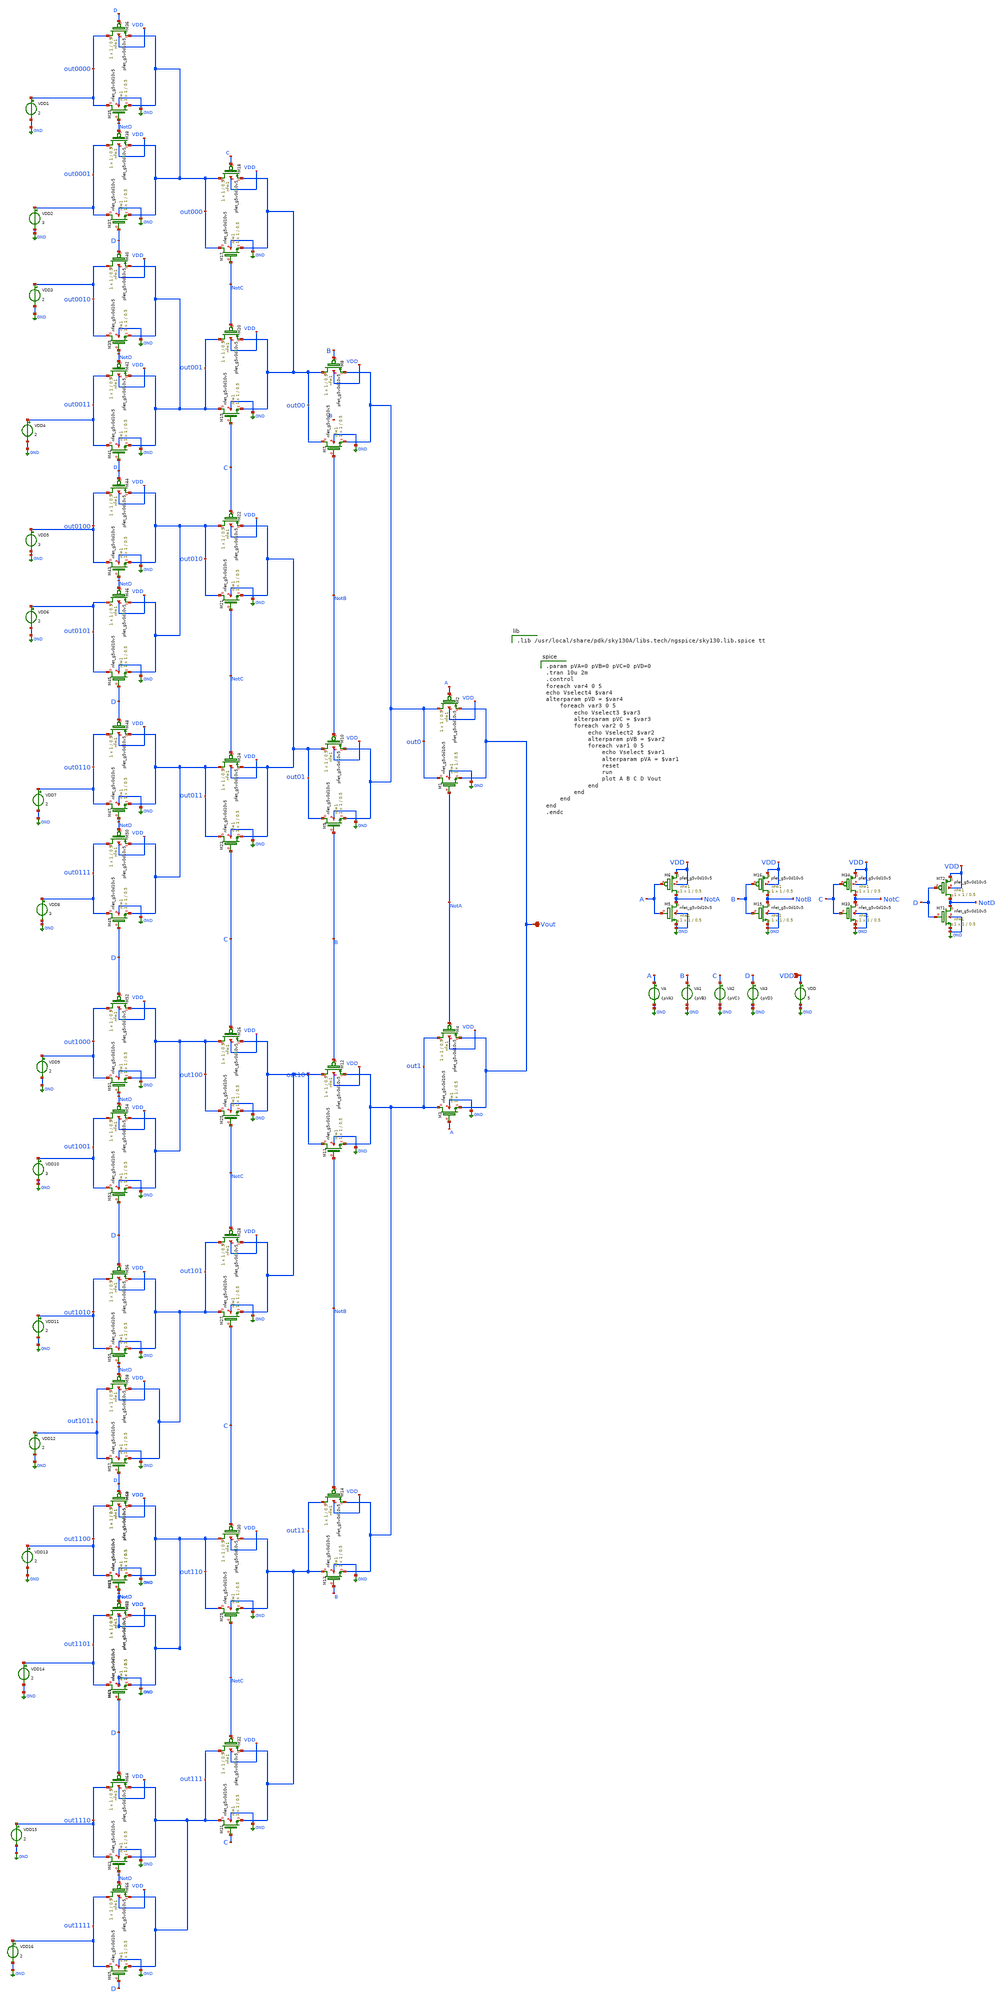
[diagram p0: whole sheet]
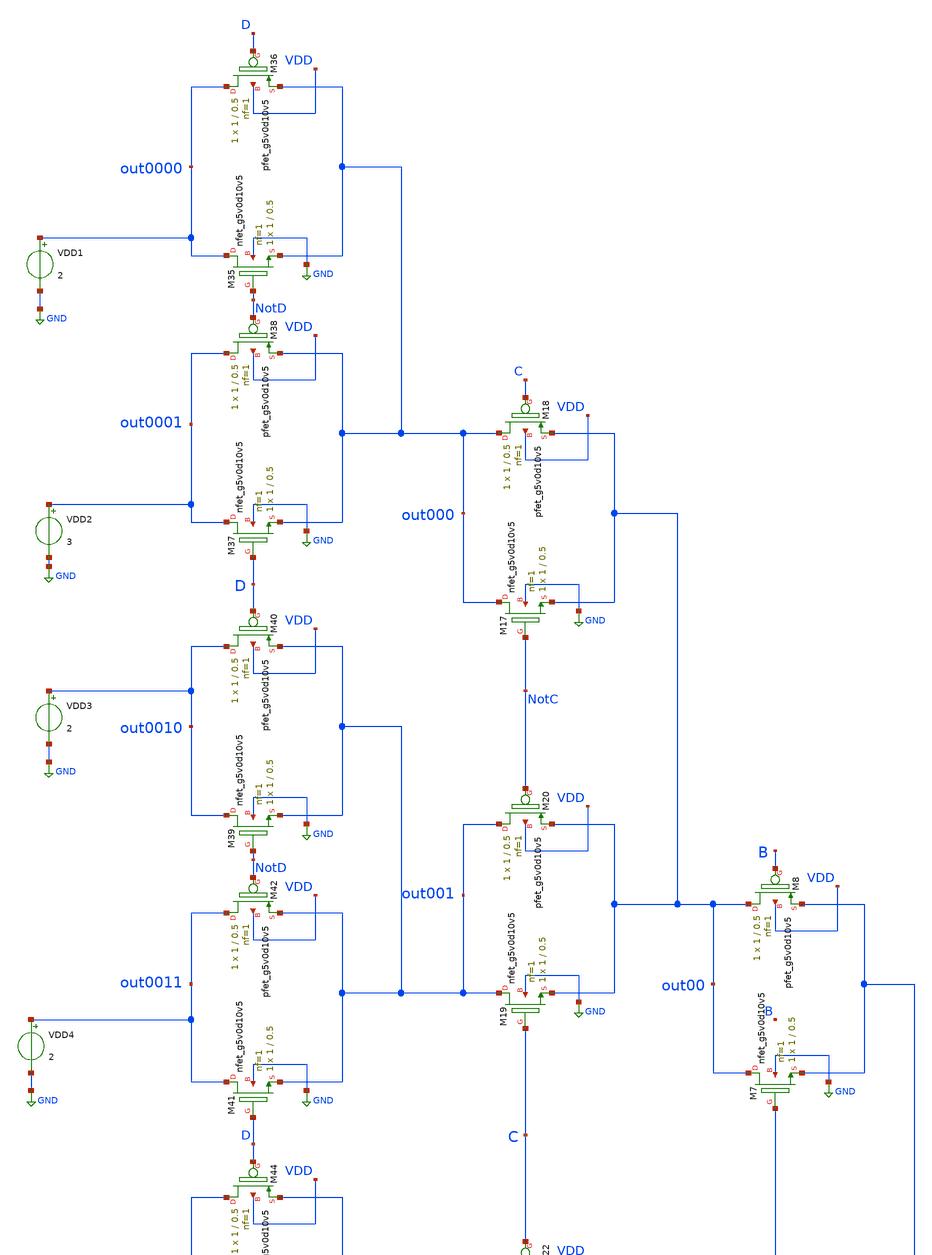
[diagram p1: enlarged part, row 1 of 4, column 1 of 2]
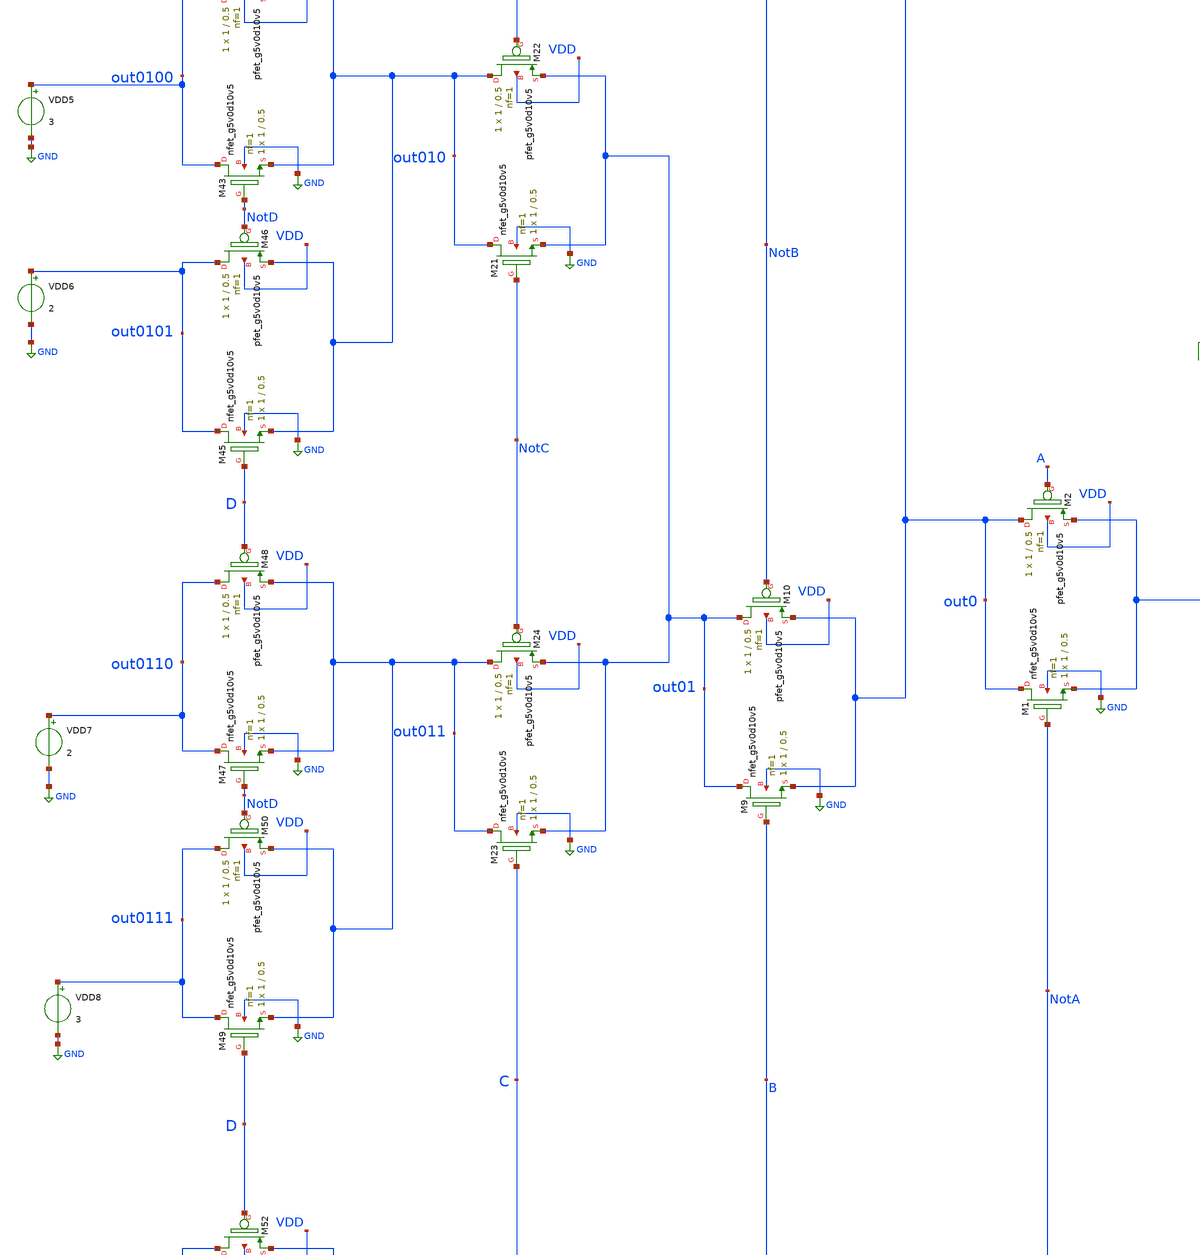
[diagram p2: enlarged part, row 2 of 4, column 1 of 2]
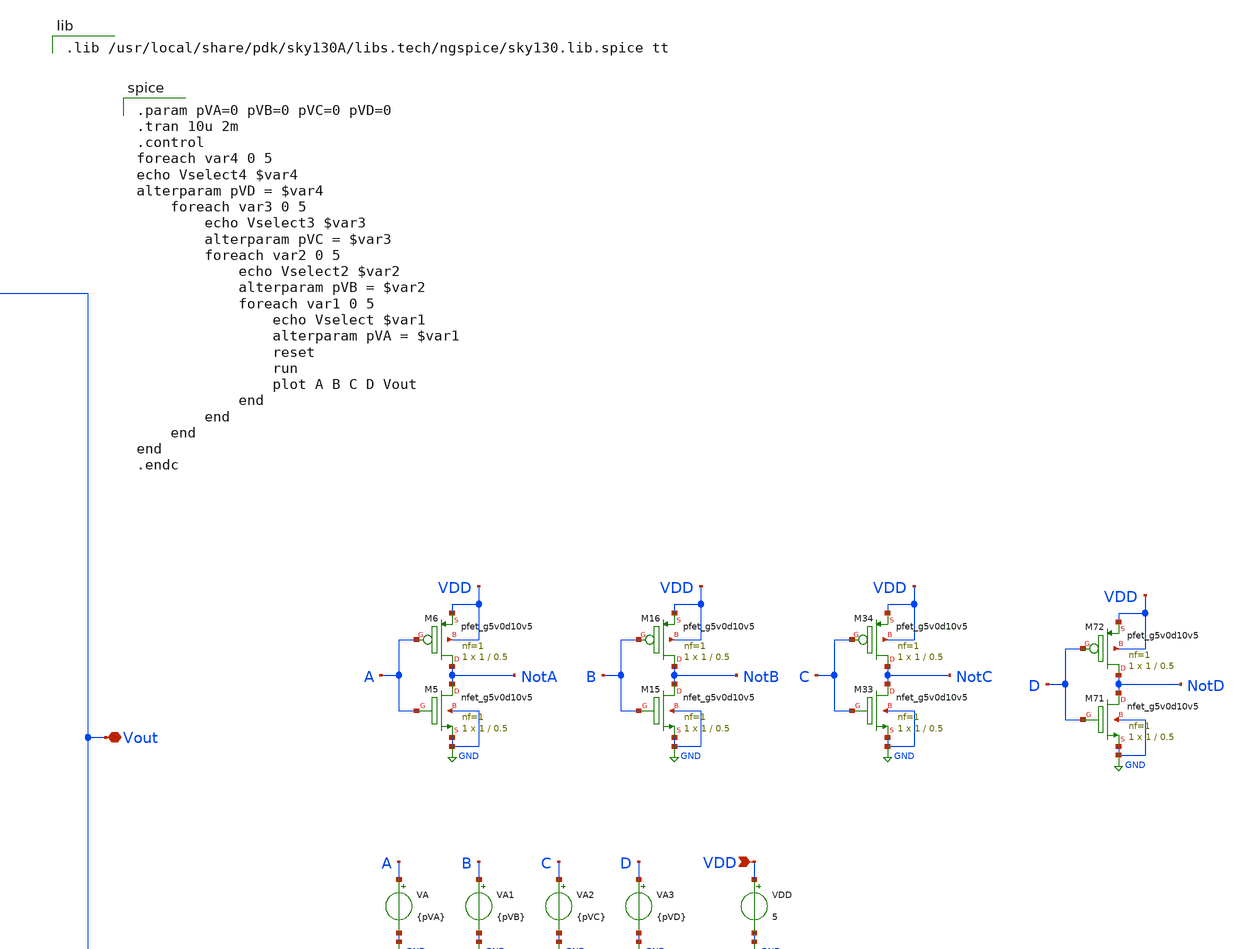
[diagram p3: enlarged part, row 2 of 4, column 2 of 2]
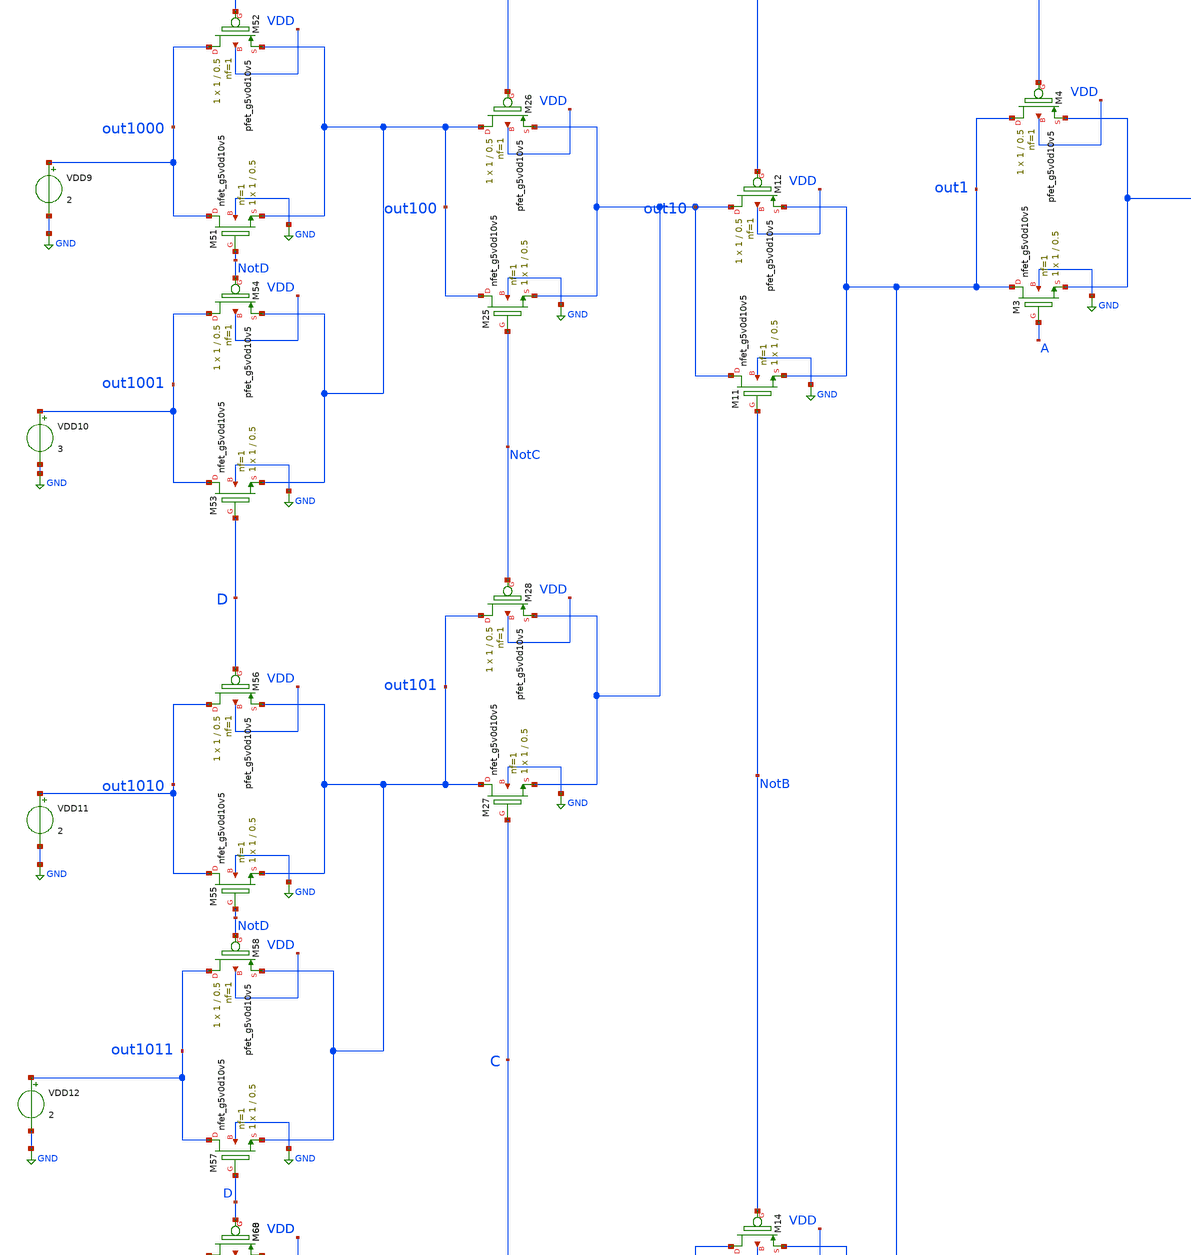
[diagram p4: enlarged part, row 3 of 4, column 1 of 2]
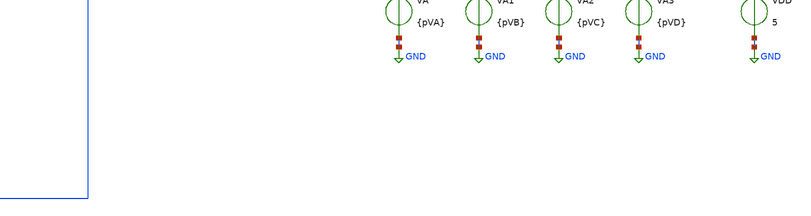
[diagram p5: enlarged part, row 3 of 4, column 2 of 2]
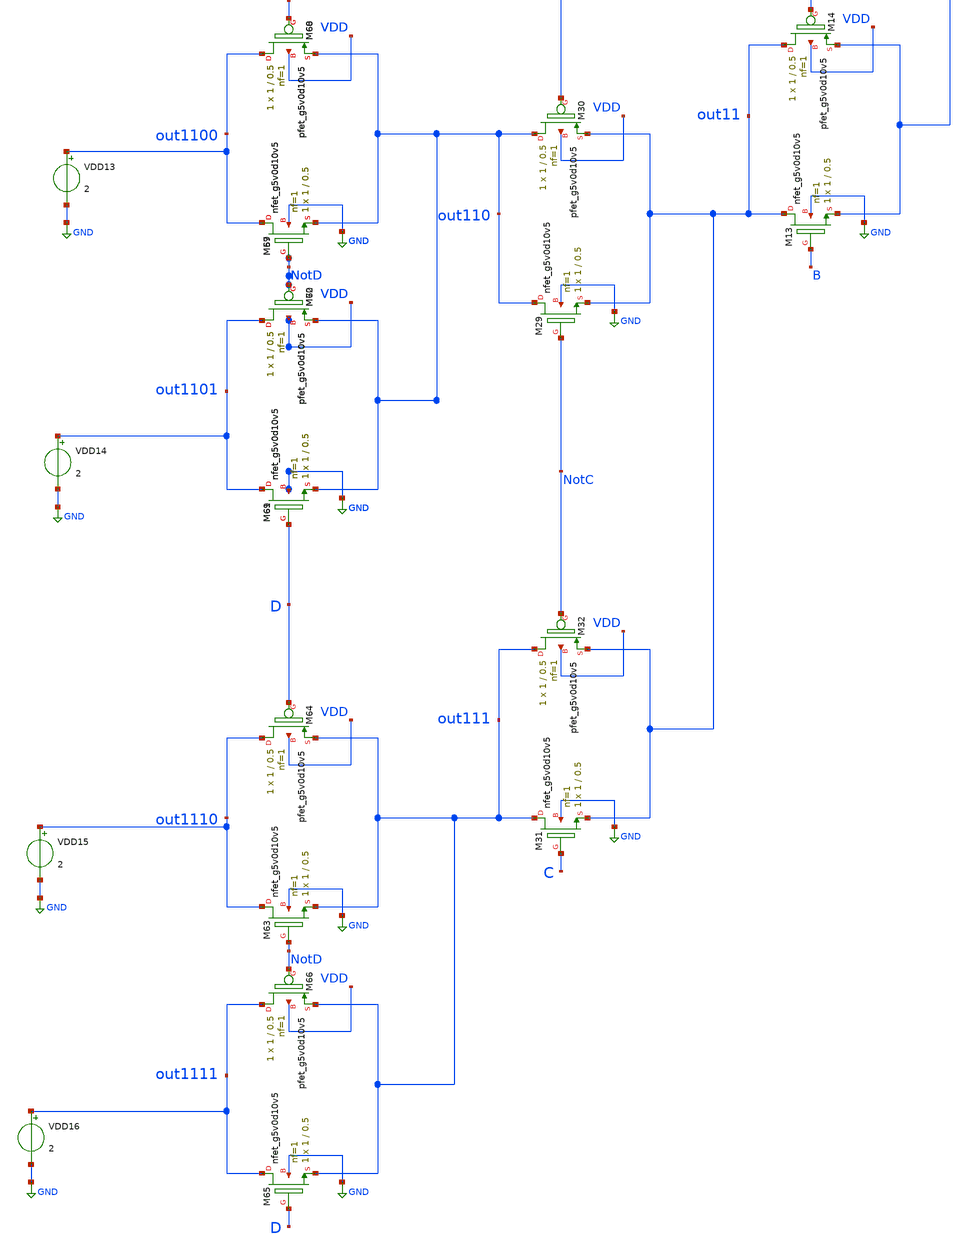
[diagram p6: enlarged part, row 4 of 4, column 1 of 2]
** sch_path: xschem/DemuxCompleto.sch
**.subckt DemuxCompleto Vout VDD
*.iopin Vout
*.ipin VDD
XM1 out0 NotA Vout GND sky130_fd_pr__nfet_g5v0d10v5 L=0.5 W=1 nf=1 ad='int((nf+1)/2) * W/nf * 0.29' as='int((nf+2)/2) * W/nf * 0.29'
+ pd='2*int((nf+1)/2) * (W/nf + 0.29)' ps='2*int((nf+2)/2) * (W/nf + 0.29)' nrd='0.29 / W' nrs='0.29 / W'
+ sa=0 sb=0 sd=0 mult=1 m=1
XM2 out0 A Vout VDD sky130_fd_pr__pfet_g5v0d10v5 L=0.5 W=1 nf=1 ad='int((nf+1)/2) * W/nf * 0.29' as='int((nf+2)/2) * W/nf * 0.29'
+ pd='2*int((nf+1)/2) * (W/nf + 0.29)' ps='2*int((nf+2)/2) * (W/nf + 0.29)' nrd='0.29 / W' nrs='0.29 / W'
+ sa=0 sb=0 sd=0 mult=1 m=1
XM3 out1 A Vout GND sky130_fd_pr__nfet_g5v0d10v5 L=0.5 W=1 nf=1 ad='int((nf+1)/2) * W/nf * 0.29' as='int((nf+2)/2) * W/nf * 0.29'
+ pd='2*int((nf+1)/2) * (W/nf + 0.29)' ps='2*int((nf+2)/2) * (W/nf + 0.29)' nrd='0.29 / W' nrs='0.29 / W'
+ sa=0 sb=0 sd=0 mult=1 m=1
XM4 out1 NotA Vout VDD sky130_fd_pr__pfet_g5v0d10v5 L=0.5 W=1 nf=1 ad='int((nf+1)/2) * W/nf * 0.29' as='int((nf+2)/2) * W/nf * 0.29'
+ pd='2*int((nf+1)/2) * (W/nf + 0.29)' ps='2*int((nf+2)/2) * (W/nf + 0.29)' nrd='0.29 / W' nrs='0.29 / W'
+ sa=0 sb=0 sd=0 mult=1 m=1
XM5 NotA A GND GND sky130_fd_pr__nfet_g5v0d10v5 L=0.5 W=1 nf=1 ad='int((nf+1)/2) * W/nf * 0.29' as='int((nf+2)/2) * W/nf * 0.29'
+ pd='2*int((nf+1)/2) * (W/nf + 0.29)' ps='2*int((nf+2)/2) * (W/nf + 0.29)' nrd='0.29 / W' nrs='0.29 / W'
+ sa=0 sb=0 sd=0 mult=1 m=1
XM6 NotA A VDD VDD sky130_fd_pr__pfet_g5v0d10v5 L=0.5 W=1 nf=1 ad='int((nf+1)/2) * W/nf * 0.29' as='int((nf+2)/2) * W/nf * 0.29'
+ pd='2*int((nf+1)/2) * (W/nf + 0.29)' ps='2*int((nf+2)/2) * (W/nf + 0.29)' nrd='0.29 / W' nrs='0.29 / W'
+ sa=0 sb=0 sd=0 mult=1 m=1
VA A GND {pVA}
VDD VDD GND 5
VDD1 out0000 GND 2
VDD2 out0001 GND 3
XM7 out00 NotB out0 GND sky130_fd_pr__nfet_g5v0d10v5 L=0.5 W=1 nf=1 ad='int((nf+1)/2) * W/nf * 0.29'
+ as='int((nf+2)/2) * W/nf * 0.29' pd='2*int((nf+1)/2) * (W/nf + 0.29)' ps='2*int((nf+2)/2) * (W/nf + 0.29)'
+ nrd='0.29 / W' nrs='0.29 / W' sa=0 sb=0 sd=0 mult=1 m=1
XM8 out00 B out0 VDD sky130_fd_pr__pfet_g5v0d10v5 L=0.5 W=1 nf=1 ad='int((nf+1)/2) * W/nf * 0.29' as='int((nf+2)/2) * W/nf * 0.29'
+ pd='2*int((nf+1)/2) * (W/nf + 0.29)' ps='2*int((nf+2)/2) * (W/nf + 0.29)' nrd='0.29 / W' nrs='0.29 / W'
+ sa=0 sb=0 sd=0 mult=1 m=1
XM9 out01 B out0 GND sky130_fd_pr__nfet_g5v0d10v5 L=0.5 W=1 nf=1 ad='int((nf+1)/2) * W/nf * 0.29' as='int((nf+2)/2) * W/nf * 0.29'
+ pd='2*int((nf+1)/2) * (W/nf + 0.29)' ps='2*int((nf+2)/2) * (W/nf + 0.29)' nrd='0.29 / W' nrs='0.29 / W'
+ sa=0 sb=0 sd=0 mult=1 m=1
XM10 out01 NotB out0 VDD sky130_fd_pr__pfet_g5v0d10v5 L=0.5 W=1 nf=1 ad='int((nf+1)/2) * W/nf * 0.29'
+ as='int((nf+2)/2) * W/nf * 0.29' pd='2*int((nf+1)/2) * (W/nf + 0.29)' ps='2*int((nf+2)/2) * (W/nf + 0.29)'
+ nrd='0.29 / W' nrs='0.29 / W' sa=0 sb=0 sd=0 mult=1 m=1
XM11 out10 NotB out1 GND sky130_fd_pr__nfet_g5v0d10v5 L=0.5 W=1 nf=1 ad='int((nf+1)/2) * W/nf * 0.29'
+ as='int((nf+2)/2) * W/nf * 0.29' pd='2*int((nf+1)/2) * (W/nf + 0.29)' ps='2*int((nf+2)/2) * (W/nf + 0.29)'
+ nrd='0.29 / W' nrs='0.29 / W' sa=0 sb=0 sd=0 mult=1 m=1
XM12 out10 B out1 VDD sky130_fd_pr__pfet_g5v0d10v5 L=0.5 W=1 nf=1 ad='int((nf+1)/2) * W/nf * 0.29' as='int((nf+2)/2) * W/nf * 0.29'
+ pd='2*int((nf+1)/2) * (W/nf + 0.29)' ps='2*int((nf+2)/2) * (W/nf + 0.29)' nrd='0.29 / W' nrs='0.29 / W'
+ sa=0 sb=0 sd=0 mult=1 m=1
XM13 out11 B out1 GND sky130_fd_pr__nfet_g5v0d10v5 L=0.5 W=1 nf=1 ad='int((nf+1)/2) * W/nf * 0.29' as='int((nf+2)/2) * W/nf * 0.29'
+ pd='2*int((nf+1)/2) * (W/nf + 0.29)' ps='2*int((nf+2)/2) * (W/nf + 0.29)' nrd='0.29 / W' nrs='0.29 / W'
+ sa=0 sb=0 sd=0 mult=1 m=1
XM14 out11 NotB out1 VDD sky130_fd_pr__pfet_g5v0d10v5 L=0.5 W=1 nf=1 ad='int((nf+1)/2) * W/nf * 0.29'
+ as='int((nf+2)/2) * W/nf * 0.29' pd='2*int((nf+1)/2) * (W/nf + 0.29)' ps='2*int((nf+2)/2) * (W/nf + 0.29)'
+ nrd='0.29 / W' nrs='0.29 / W' sa=0 sb=0 sd=0 mult=1 m=1
XM15 NotB B GND GND sky130_fd_pr__nfet_g5v0d10v5 L=0.5 W=1 nf=1 ad='int((nf+1)/2) * W/nf * 0.29' as='int((nf+2)/2) * W/nf * 0.29'
+ pd='2*int((nf+1)/2) * (W/nf + 0.29)' ps='2*int((nf+2)/2) * (W/nf + 0.29)' nrd='0.29 / W' nrs='0.29 / W'
+ sa=0 sb=0 sd=0 mult=1 m=1
XM16 NotB B VDD VDD sky130_fd_pr__pfet_g5v0d10v5 L=0.5 W=1 nf=1 ad='int((nf+1)/2) * W/nf * 0.29' as='int((nf+2)/2) * W/nf * 0.29'
+ pd='2*int((nf+1)/2) * (W/nf + 0.29)' ps='2*int((nf+2)/2) * (W/nf + 0.29)' nrd='0.29 / W' nrs='0.29 / W'
+ sa=0 sb=0 sd=0 mult=1 m=1
VA1 B GND {pVB}
VDD3 out0010 GND 2
XM17 out000 NotC out00 GND sky130_fd_pr__nfet_g5v0d10v5 L=0.5 W=1 nf=1 ad='int((nf+1)/2) * W/nf * 0.29'
+ as='int((nf+2)/2) * W/nf * 0.29' pd='2*int((nf+1)/2) * (W/nf + 0.29)' ps='2*int((nf+2)/2) * (W/nf + 0.29)'
+ nrd='0.29 / W' nrs='0.29 / W' sa=0 sb=0 sd=0 mult=1 m=1
XM18 out000 C out00 VDD sky130_fd_pr__pfet_g5v0d10v5 L=0.5 W=1 nf=1 ad='int((nf+1)/2) * W/nf * 0.29'
+ as='int((nf+2)/2) * W/nf * 0.29' pd='2*int((nf+1)/2) * (W/nf + 0.29)' ps='2*int((nf+2)/2) * (W/nf + 0.29)'
+ nrd='0.29 / W' nrs='0.29 / W' sa=0 sb=0 sd=0 mult=1 m=1
XM19 out001 C out00 GND sky130_fd_pr__nfet_g5v0d10v5 L=0.5 W=1 nf=1 ad='int((nf+1)/2) * W/nf * 0.29'
+ as='int((nf+2)/2) * W/nf * 0.29' pd='2*int((nf+1)/2) * (W/nf + 0.29)' ps='2*int((nf+2)/2) * (W/nf + 0.29)'
+ nrd='0.29 / W' nrs='0.29 / W' sa=0 sb=0 sd=0 mult=1 m=1
XM20 out001 NotC out00 VDD sky130_fd_pr__pfet_g5v0d10v5 L=0.5 W=1 nf=1 ad='int((nf+1)/2) * W/nf * 0.29'
+ as='int((nf+2)/2) * W/nf * 0.29' pd='2*int((nf+1)/2) * (W/nf + 0.29)' ps='2*int((nf+2)/2) * (W/nf + 0.29)'
+ nrd='0.29 / W' nrs='0.29 / W' sa=0 sb=0 sd=0 mult=1 m=1
XM21 out010 NotC out01 GND sky130_fd_pr__nfet_g5v0d10v5 L=0.5 W=1 nf=1 ad='int((nf+1)/2) * W/nf * 0.29'
+ as='int((nf+2)/2) * W/nf * 0.29' pd='2*int((nf+1)/2) * (W/nf + 0.29)' ps='2*int((nf+2)/2) * (W/nf + 0.29)'
+ nrd='0.29 / W' nrs='0.29 / W' sa=0 sb=0 sd=0 mult=1 m=1
XM22 out010 C out01 VDD sky130_fd_pr__pfet_g5v0d10v5 L=0.5 W=1 nf=1 ad='int((nf+1)/2) * W/nf * 0.29'
+ as='int((nf+2)/2) * W/nf * 0.29' pd='2*int((nf+1)/2) * (W/nf + 0.29)' ps='2*int((nf+2)/2) * (W/nf + 0.29)'
+ nrd='0.29 / W' nrs='0.29 / W' sa=0 sb=0 sd=0 mult=1 m=1
XM23 out011 C out01 GND sky130_fd_pr__nfet_g5v0d10v5 L=0.5 W=1 nf=1 ad='int((nf+1)/2) * W/nf * 0.29'
+ as='int((nf+2)/2) * W/nf * 0.29' pd='2*int((nf+1)/2) * (W/nf + 0.29)' ps='2*int((nf+2)/2) * (W/nf + 0.29)'
+ nrd='0.29 / W' nrs='0.29 / W' sa=0 sb=0 sd=0 mult=1 m=1
XM24 out011 NotC out01 VDD sky130_fd_pr__pfet_g5v0d10v5 L=0.5 W=1 nf=1 ad='int((nf+1)/2) * W/nf * 0.29'
+ as='int((nf+2)/2) * W/nf * 0.29' pd='2*int((nf+1)/2) * (W/nf + 0.29)' ps='2*int((nf+2)/2) * (W/nf + 0.29)'
+ nrd='0.29 / W' nrs='0.29 / W' sa=0 sb=0 sd=0 mult=1 m=1
XM25 out100 NotC out10 GND sky130_fd_pr__nfet_g5v0d10v5 L=0.5 W=1 nf=1 ad='int((nf+1)/2) * W/nf * 0.29'
+ as='int((nf+2)/2) * W/nf * 0.29' pd='2*int((nf+1)/2) * (W/nf + 0.29)' ps='2*int((nf+2)/2) * (W/nf + 0.29)'
+ nrd='0.29 / W' nrs='0.29 / W' sa=0 sb=0 sd=0 mult=1 m=1
XM26 out100 C out10 VDD sky130_fd_pr__pfet_g5v0d10v5 L=0.5 W=1 nf=1 ad='int((nf+1)/2) * W/nf * 0.29'
+ as='int((nf+2)/2) * W/nf * 0.29' pd='2*int((nf+1)/2) * (W/nf + 0.29)' ps='2*int((nf+2)/2) * (W/nf + 0.29)'
+ nrd='0.29 / W' nrs='0.29 / W' sa=0 sb=0 sd=0 mult=1 m=1
XM27 out101 C out10 GND sky130_fd_pr__nfet_g5v0d10v5 L=0.5 W=1 nf=1 ad='int((nf+1)/2) * W/nf * 0.29'
+ as='int((nf+2)/2) * W/nf * 0.29' pd='2*int((nf+1)/2) * (W/nf + 0.29)' ps='2*int((nf+2)/2) * (W/nf + 0.29)'
+ nrd='0.29 / W' nrs='0.29 / W' sa=0 sb=0 sd=0 mult=1 m=1
XM28 out101 NotC out10 VDD sky130_fd_pr__pfet_g5v0d10v5 L=0.5 W=1 nf=1 ad='int((nf+1)/2) * W/nf * 0.29'
+ as='int((nf+2)/2) * W/nf * 0.29' pd='2*int((nf+1)/2) * (W/nf + 0.29)' ps='2*int((nf+2)/2) * (W/nf + 0.29)'
+ nrd='0.29 / W' nrs='0.29 / W' sa=0 sb=0 sd=0 mult=1 m=1
XM29 out110 NotC out11 GND sky130_fd_pr__nfet_g5v0d10v5 L=0.5 W=1 nf=1 ad='int((nf+1)/2) * W/nf * 0.29'
+ as='int((nf+2)/2) * W/nf * 0.29' pd='2*int((nf+1)/2) * (W/nf + 0.29)' ps='2*int((nf+2)/2) * (W/nf + 0.29)'
+ nrd='0.29 / W' nrs='0.29 / W' sa=0 sb=0 sd=0 mult=1 m=1
XM30 out110 C out11 VDD sky130_fd_pr__pfet_g5v0d10v5 L=0.5 W=1 nf=1 ad='int((nf+1)/2) * W/nf * 0.29'
+ as='int((nf+2)/2) * W/nf * 0.29' pd='2*int((nf+1)/2) * (W/nf + 0.29)' ps='2*int((nf+2)/2) * (W/nf + 0.29)'
+ nrd='0.29 / W' nrs='0.29 / W' sa=0 sb=0 sd=0 mult=1 m=1
XM31 out111 C out11 GND sky130_fd_pr__nfet_g5v0d10v5 L=0.5 W=1 nf=1 ad='int((nf+1)/2) * W/nf * 0.29'
+ as='int((nf+2)/2) * W/nf * 0.29' pd='2*int((nf+1)/2) * (W/nf + 0.29)' ps='2*int((nf+2)/2) * (W/nf + 0.29)'
+ nrd='0.29 / W' nrs='0.29 / W' sa=0 sb=0 sd=0 mult=1 m=1
XM32 out111 NotC out11 VDD sky130_fd_pr__pfet_g5v0d10v5 L=0.5 W=1 nf=1 ad='int((nf+1)/2) * W/nf * 0.29'
+ as='int((nf+2)/2) * W/nf * 0.29' pd='2*int((nf+1)/2) * (W/nf + 0.29)' ps='2*int((nf+2)/2) * (W/nf + 0.29)'
+ nrd='0.29 / W' nrs='0.29 / W' sa=0 sb=0 sd=0 mult=1 m=1
XM33 NotC C GND GND sky130_fd_pr__nfet_g5v0d10v5 L=0.5 W=1 nf=1 ad='int((nf+1)/2) * W/nf * 0.29' as='int((nf+2)/2) * W/nf * 0.29'
+ pd='2*int((nf+1)/2) * (W/nf + 0.29)' ps='2*int((nf+2)/2) * (W/nf + 0.29)' nrd='0.29 / W' nrs='0.29 / W'
+ sa=0 sb=0 sd=0 mult=1 m=1
XM34 NotC C VDD VDD sky130_fd_pr__pfet_g5v0d10v5 L=0.5 W=1 nf=1 ad='int((nf+1)/2) * W/nf * 0.29' as='int((nf+2)/2) * W/nf * 0.29'
+ pd='2*int((nf+1)/2) * (W/nf + 0.29)' ps='2*int((nf+2)/2) * (W/nf + 0.29)' nrd='0.29 / W' nrs='0.29 / W'
+ sa=0 sb=0 sd=0 mult=1 m=1
XM35 out0000 NotD out000 GND sky130_fd_pr__nfet_g5v0d10v5 L=0.5 W=1 nf=1 ad='int((nf+1)/2) * W/nf * 0.29'
+ as='int((nf+2)/2) * W/nf * 0.29' pd='2*int((nf+1)/2) * (W/nf + 0.29)' ps='2*int((nf+2)/2) * (W/nf + 0.29)'
+ nrd='0.29 / W' nrs='0.29 / W' sa=0 sb=0 sd=0 mult=1 m=1
XM36 out0000 D out000 VDD sky130_fd_pr__pfet_g5v0d10v5 L=0.5 W=1 nf=1 ad='int((nf+1)/2) * W/nf * 0.29'
+ as='int((nf+2)/2) * W/nf * 0.29' pd='2*int((nf+1)/2) * (W/nf + 0.29)' ps='2*int((nf+2)/2) * (W/nf + 0.29)'
+ nrd='0.29 / W' nrs='0.29 / W' sa=0 sb=0 sd=0 mult=1 m=1
XM37 out0001 D out000 GND sky130_fd_pr__nfet_g5v0d10v5 L=0.5 W=1 nf=1 ad='int((nf+1)/2) * W/nf * 0.29'
+ as='int((nf+2)/2) * W/nf * 0.29' pd='2*int((nf+1)/2) * (W/nf + 0.29)' ps='2*int((nf+2)/2) * (W/nf + 0.29)'
+ nrd='0.29 / W' nrs='0.29 / W' sa=0 sb=0 sd=0 mult=1 m=1
XM38 out0001 NotD out000 VDD sky130_fd_pr__pfet_g5v0d10v5 L=0.5 W=1 nf=1 ad='int((nf+1)/2) * W/nf * 0.29'
+ as='int((nf+2)/2) * W/nf * 0.29' pd='2*int((nf+1)/2) * (W/nf + 0.29)' ps='2*int((nf+2)/2) * (W/nf + 0.29)'
+ nrd='0.29 / W' nrs='0.29 / W' sa=0 sb=0 sd=0 mult=1 m=1
XM39 out0010 NotD out001 GND sky130_fd_pr__nfet_g5v0d10v5 L=0.5 W=1 nf=1 ad='int((nf+1)/2) * W/nf * 0.29'
+ as='int((nf+2)/2) * W/nf * 0.29' pd='2*int((nf+1)/2) * (W/nf + 0.29)' ps='2*int((nf+2)/2) * (W/nf + 0.29)'
+ nrd='0.29 / W' nrs='0.29 / W' sa=0 sb=0 sd=0 mult=1 m=1
XM40 out0010 D out001 VDD sky130_fd_pr__pfet_g5v0d10v5 L=0.5 W=1 nf=1 ad='int((nf+1)/2) * W/nf * 0.29'
+ as='int((nf+2)/2) * W/nf * 0.29' pd='2*int((nf+1)/2) * (W/nf + 0.29)' ps='2*int((nf+2)/2) * (W/nf + 0.29)'
+ nrd='0.29 / W' nrs='0.29 / W' sa=0 sb=0 sd=0 mult=1 m=1
XM41 out0011 D out001 GND sky130_fd_pr__nfet_g5v0d10v5 L=0.5 W=1 nf=1 ad='int((nf+1)/2) * W/nf * 0.29'
+ as='int((nf+2)/2) * W/nf * 0.29' pd='2*int((nf+1)/2) * (W/nf + 0.29)' ps='2*int((nf+2)/2) * (W/nf + 0.29)'
+ nrd='0.29 / W' nrs='0.29 / W' sa=0 sb=0 sd=0 mult=1 m=1
XM42 out0011 NotD out001 VDD sky130_fd_pr__pfet_g5v0d10v5 L=0.5 W=1 nf=1 ad='int((nf+1)/2) * W/nf * 0.29'
+ as='int((nf+2)/2) * W/nf * 0.29' pd='2*int((nf+1)/2) * (W/nf + 0.29)' ps='2*int((nf+2)/2) * (W/nf + 0.29)'
+ nrd='0.29 / W' nrs='0.29 / W' sa=0 sb=0 sd=0 mult=1 m=1
XM43 out0100 NotD out010 GND sky130_fd_pr__nfet_g5v0d10v5 L=0.5 W=1 nf=1 ad='int((nf+1)/2) * W/nf * 0.29'
+ as='int((nf+2)/2) * W/nf * 0.29' pd='2*int((nf+1)/2) * (W/nf + 0.29)' ps='2*int((nf+2)/2) * (W/nf + 0.29)'
+ nrd='0.29 / W' nrs='0.29 / W' sa=0 sb=0 sd=0 mult=1 m=1
XM44 out0100 D out010 VDD sky130_fd_pr__pfet_g5v0d10v5 L=0.5 W=1 nf=1 ad='int((nf+1)/2) * W/nf * 0.29'
+ as='int((nf+2)/2) * W/nf * 0.29' pd='2*int((nf+1)/2) * (W/nf + 0.29)' ps='2*int((nf+2)/2) * (W/nf + 0.29)'
+ nrd='0.29 / W' nrs='0.29 / W' sa=0 sb=0 sd=0 mult=1 m=1
XM45 out0101 D out010 GND sky130_fd_pr__nfet_g5v0d10v5 L=0.5 W=1 nf=1 ad='int((nf+1)/2) * W/nf * 0.29'
+ as='int((nf+2)/2) * W/nf * 0.29' pd='2*int((nf+1)/2) * (W/nf + 0.29)' ps='2*int((nf+2)/2) * (W/nf + 0.29)'
+ nrd='0.29 / W' nrs='0.29 / W' sa=0 sb=0 sd=0 mult=1 m=1
XM46 out0101 NotD out010 VDD sky130_fd_pr__pfet_g5v0d10v5 L=0.5 W=1 nf=1 ad='int((nf+1)/2) * W/nf * 0.29'
+ as='int((nf+2)/2) * W/nf * 0.29' pd='2*int((nf+1)/2) * (W/nf + 0.29)' ps='2*int((nf+2)/2) * (W/nf + 0.29)'
+ nrd='0.29 / W' nrs='0.29 / W' sa=0 sb=0 sd=0 mult=1 m=1
XM47 out0110 NotD out011 GND sky130_fd_pr__nfet_g5v0d10v5 L=0.5 W=1 nf=1 ad='int((nf+1)/2) * W/nf * 0.29'
+ as='int((nf+2)/2) * W/nf * 0.29' pd='2*int((nf+1)/2) * (W/nf + 0.29)' ps='2*int((nf+2)/2) * (W/nf + 0.29)'
+ nrd='0.29 / W' nrs='0.29 / W' sa=0 sb=0 sd=0 mult=1 m=1
XM48 out0110 D out011 VDD sky130_fd_pr__pfet_g5v0d10v5 L=0.5 W=1 nf=1 ad='int((nf+1)/2) * W/nf * 0.29'
+ as='int((nf+2)/2) * W/nf * 0.29' pd='2*int((nf+1)/2) * (W/nf + 0.29)' ps='2*int((nf+2)/2) * (W/nf + 0.29)'
+ nrd='0.29 / W' nrs='0.29 / W' sa=0 sb=0 sd=0 mult=1 m=1
XM49 out0111 D out011 GND sky130_fd_pr__nfet_g5v0d10v5 L=0.5 W=1 nf=1 ad='int((nf+1)/2) * W/nf * 0.29'
+ as='int((nf+2)/2) * W/nf * 0.29' pd='2*int((nf+1)/2) * (W/nf + 0.29)' ps='2*int((nf+2)/2) * (W/nf + 0.29)'
+ nrd='0.29 / W' nrs='0.29 / W' sa=0 sb=0 sd=0 mult=1 m=1
XM50 out0111 NotD out011 VDD sky130_fd_pr__pfet_g5v0d10v5 L=0.5 W=1 nf=1 ad='int((nf+1)/2) * W/nf * 0.29'
+ as='int((nf+2)/2) * W/nf * 0.29' pd='2*int((nf+1)/2) * (W/nf + 0.29)' ps='2*int((nf+2)/2) * (W/nf + 0.29)'
+ nrd='0.29 / W' nrs='0.29 / W' sa=0 sb=0 sd=0 mult=1 m=1
XM51 out1000 NotD out100 GND sky130_fd_pr__nfet_g5v0d10v5 L=0.5 W=1 nf=1 ad='int((nf+1)/2) * W/nf * 0.29'
+ as='int((nf+2)/2) * W/nf * 0.29' pd='2*int((nf+1)/2) * (W/nf + 0.29)' ps='2*int((nf+2)/2) * (W/nf + 0.29)'
+ nrd='0.29 / W' nrs='0.29 / W' sa=0 sb=0 sd=0 mult=1 m=1
XM52 out1000 D out100 VDD sky130_fd_pr__pfet_g5v0d10v5 L=0.5 W=1 nf=1 ad='int((nf+1)/2) * W/nf * 0.29'
+ as='int((nf+2)/2) * W/nf * 0.29' pd='2*int((nf+1)/2) * (W/nf + 0.29)' ps='2*int((nf+2)/2) * (W/nf + 0.29)'
+ nrd='0.29 / W' nrs='0.29 / W' sa=0 sb=0 sd=0 mult=1 m=1
XM53 out1001 D out100 GND sky130_fd_pr__nfet_g5v0d10v5 L=0.5 W=1 nf=1 ad='int((nf+1)/2) * W/nf * 0.29'
+ as='int((nf+2)/2) * W/nf * 0.29' pd='2*int((nf+1)/2) * (W/nf + 0.29)' ps='2*int((nf+2)/2) * (W/nf + 0.29)'
+ nrd='0.29 / W' nrs='0.29 / W' sa=0 sb=0 sd=0 mult=1 m=1
XM54 out1001 NotD out100 VDD sky130_fd_pr__pfet_g5v0d10v5 L=0.5 W=1 nf=1 ad='int((nf+1)/2) * W/nf * 0.29'
+ as='int((nf+2)/2) * W/nf * 0.29' pd='2*int((nf+1)/2) * (W/nf + 0.29)' ps='2*int((nf+2)/2) * (W/nf + 0.29)'
+ nrd='0.29 / W' nrs='0.29 / W' sa=0 sb=0 sd=0 mult=1 m=1
XM55 out1010 NotD out101 GND sky130_fd_pr__nfet_g5v0d10v5 L=0.5 W=1 nf=1 ad='int((nf+1)/2) * W/nf * 0.29'
+ as='int((nf+2)/2) * W/nf * 0.29' pd='2*int((nf+1)/2) * (W/nf + 0.29)' ps='2*int((nf+2)/2) * (W/nf + 0.29)'
+ nrd='0.29 / W' nrs='0.29 / W' sa=0 sb=0 sd=0 mult=1 m=1
XM56 out1010 D out101 VDD sky130_fd_pr__pfet_g5v0d10v5 L=0.5 W=1 nf=1 ad='int((nf+1)/2) * W/nf * 0.29'
+ as='int((nf+2)/2) * W/nf * 0.29' pd='2*int((nf+1)/2) * (W/nf + 0.29)' ps='2*int((nf+2)/2) * (W/nf + 0.29)'
+ nrd='0.29 / W' nrs='0.29 / W' sa=0 sb=0 sd=0 mult=1 m=1
XM57 out1011 D out101 GND sky130_fd_pr__nfet_g5v0d10v5 L=0.5 W=1 nf=1 ad='int((nf+1)/2) * W/nf * 0.29'
+ as='int((nf+2)/2) * W/nf * 0.29' pd='2*int((nf+1)/2) * (W/nf + 0.29)' ps='2*int((nf+2)/2) * (W/nf + 0.29)'
+ nrd='0.29 / W' nrs='0.29 / W' sa=0 sb=0 sd=0 mult=1 m=1
XM58 out1011 NotD out101 VDD sky130_fd_pr__pfet_g5v0d10v5 L=0.5 W=1 nf=1 ad='int((nf+1)/2) * W/nf * 0.29'
+ as='int((nf+2)/2) * W/nf * 0.29' pd='2*int((nf+1)/2) * (W/nf + 0.29)' ps='2*int((nf+2)/2) * (W/nf + 0.29)'
+ nrd='0.29 / W' nrs='0.29 / W' sa=0 sb=0 sd=0 mult=1 m=1
XM59 out1100 NotD out110 GND sky130_fd_pr__nfet_g5v0d10v5 L=0.5 W=1 nf=1 ad='int((nf+1)/2) * W/nf * 0.29'
+ as='int((nf+2)/2) * W/nf * 0.29' pd='2*int((nf+1)/2) * (W/nf + 0.29)' ps='2*int((nf+2)/2) * (W/nf + 0.29)'
+ nrd='0.29 / W' nrs='0.29 / W' sa=0 sb=0 sd=0 mult=1 m=1
XM60 out1100 D out110 VDD sky130_fd_pr__pfet_g5v0d10v5 L=0.5 W=1 nf=1 ad='int((nf+1)/2) * W/nf * 0.29'
+ as='int((nf+2)/2) * W/nf * 0.29' pd='2*int((nf+1)/2) * (W/nf + 0.29)' ps='2*int((nf+2)/2) * (W/nf + 0.29)'
+ nrd='0.29 / W' nrs='0.29 / W' sa=0 sb=0 sd=0 mult=1 m=1
XM61 out1101 D out110 GND sky130_fd_pr__nfet_g5v0d10v5 L=0.5 W=1 nf=1 ad='int((nf+1)/2) * W/nf * 0.29'
+ as='int((nf+2)/2) * W/nf * 0.29' pd='2*int((nf+1)/2) * (W/nf + 0.29)' ps='2*int((nf+2)/2) * (W/nf + 0.29)'
+ nrd='0.29 / W' nrs='0.29 / W' sa=0 sb=0 sd=0 mult=1 m=1
XM62 out1101 NotD out110 VDD sky130_fd_pr__pfet_g5v0d10v5 L=0.5 W=1 nf=1 ad='int((nf+1)/2) * W/nf * 0.29'
+ as='int((nf+2)/2) * W/nf * 0.29' pd='2*int((nf+1)/2) * (W/nf + 0.29)' ps='2*int((nf+2)/2) * (W/nf + 0.29)'
+ nrd='0.29 / W' nrs='0.29 / W' sa=0 sb=0 sd=0 mult=1 m=1
XM63 out1110 NotD out111 GND sky130_fd_pr__nfet_g5v0d10v5 L=0.5 W=1 nf=1 ad='int((nf+1)/2) * W/nf * 0.29'
+ as='int((nf+2)/2) * W/nf * 0.29' pd='2*int((nf+1)/2) * (W/nf + 0.29)' ps='2*int((nf+2)/2) * (W/nf + 0.29)'
+ nrd='0.29 / W' nrs='0.29 / W' sa=0 sb=0 sd=0 mult=1 m=1
XM64 out1110 D out111 VDD sky130_fd_pr__pfet_g5v0d10v5 L=0.5 W=1 nf=1 ad='int((nf+1)/2) * W/nf * 0.29'
+ as='int((nf+2)/2) * W/nf * 0.29' pd='2*int((nf+1)/2) * (W/nf + 0.29)' ps='2*int((nf+2)/2) * (W/nf + 0.29)'
+ nrd='0.29 / W' nrs='0.29 / W' sa=0 sb=0 sd=0 mult=1 m=1
XM65 out1111 D out111 GND sky130_fd_pr__nfet_g5v0d10v5 L=0.5 W=1 nf=1 ad='int((nf+1)/2) * W/nf * 0.29'
+ as='int((nf+2)/2) * W/nf * 0.29' pd='2*int((nf+1)/2) * (W/nf + 0.29)' ps='2*int((nf+2)/2) * (W/nf + 0.29)'
+ nrd='0.29 / W' nrs='0.29 / W' sa=0 sb=0 sd=0 mult=1 m=1
XM66 out1111 NotD out111 VDD sky130_fd_pr__pfet_g5v0d10v5 L=0.5 W=1 nf=1 ad='int((nf+1)/2) * W/nf * 0.29'
+ as='int((nf+2)/2) * W/nf * 0.29' pd='2*int((nf+1)/2) * (W/nf + 0.29)' ps='2*int((nf+2)/2) * (W/nf + 0.29)'
+ nrd='0.29 / W' nrs='0.29 / W' sa=0 sb=0 sd=0 mult=1 m=1
XM67 out1100 NotD out110 GND sky130_fd_pr__nfet_g5v0d10v5 L=0.5 W=1 nf=1 ad='int((nf+1)/2) * W/nf * 0.29'
+ as='int((nf+2)/2) * W/nf * 0.29' pd='2*int((nf+1)/2) * (W/nf + 0.29)' ps='2*int((nf+2)/2) * (W/nf + 0.29)'
+ nrd='0.29 / W' nrs='0.29 / W' sa=0 sb=0 sd=0 mult=1 m=1
XM68 out1100 D out110 VDD sky130_fd_pr__pfet_g5v0d10v5 L=0.5 W=1 nf=1 ad='int((nf+1)/2) * W/nf * 0.29'
+ as='int((nf+2)/2) * W/nf * 0.29' pd='2*int((nf+1)/2) * (W/nf + 0.29)' ps='2*int((nf+2)/2) * (W/nf + 0.29)'
+ nrd='0.29 / W' nrs='0.29 / W' sa=0 sb=0 sd=0 mult=1 m=1
XM69 out1101 D out110 GND sky130_fd_pr__nfet_g5v0d10v5 L=0.5 W=1 nf=1 ad='int((nf+1)/2) * W/nf * 0.29'
+ as='int((nf+2)/2) * W/nf * 0.29' pd='2*int((nf+1)/2) * (W/nf + 0.29)' ps='2*int((nf+2)/2) * (W/nf + 0.29)'
+ nrd='0.29 / W' nrs='0.29 / W' sa=0 sb=0 sd=0 mult=1 m=1
XM70 out1101 NotD out110 VDD sky130_fd_pr__pfet_g5v0d10v5 L=0.5 W=1 nf=1 ad='int((nf+1)/2) * W/nf * 0.29'
+ as='int((nf+2)/2) * W/nf * 0.29' pd='2*int((nf+1)/2) * (W/nf + 0.29)' ps='2*int((nf+2)/2) * (W/nf + 0.29)'
+ nrd='0.29 / W' nrs='0.29 / W' sa=0 sb=0 sd=0 mult=1 m=1
XM71 NotD D GND GND sky130_fd_pr__nfet_g5v0d10v5 L=0.5 W=1 nf=1 ad='int((nf+1)/2) * W/nf * 0.29' as='int((nf+2)/2) * W/nf * 0.29'
+ pd='2*int((nf+1)/2) * (W/nf + 0.29)' ps='2*int((nf+2)/2) * (W/nf + 0.29)' nrd='0.29 / W' nrs='0.29 / W'
+ sa=0 sb=0 sd=0 mult=1 m=1
XM72 NotD D VDD VDD sky130_fd_pr__pfet_g5v0d10v5 L=0.5 W=1 nf=1 ad='int((nf+1)/2) * W/nf * 0.29' as='int((nf+2)/2) * W/nf * 0.29'
+ pd='2*int((nf+1)/2) * (W/nf + 0.29)' ps='2*int((nf+2)/2) * (W/nf + 0.29)' nrd='0.29 / W' nrs='0.29 / W'
+ sa=0 sb=0 sd=0 mult=1 m=1
VA2 C GND {pVC}
VA3 D GND {pVD}
VDD4 out0011 GND 2
VDD5 out0100 GND 3
VDD6 out0101 GND 2
VDD7 out0110 GND 2
VDD8 out0111 GND 3
VDD9 out1000 GND 2
VDD10 out1001 GND 3
VDD11 out1010 GND 2
VDD12 out1011 GND 2
VDD13 out1100 GND 2
VDD14 out1101 GND 2
VDD15 out1110 GND 2
VDD16 out1111 GND 2
**** begin user architecture code

.param pVA=0 pVB=0 pVC=0 pVD=0
.tran 10u 2m
.control
foreach var4 0 5
echo Vselect4 $var4
alterparam pVD = $var4
	foreach var3 0 5
		echo Vselect3 $var3
		alterparam pVC = $var3
		foreach var2 0 5
			echo Vselect2 $var2
			alterparam pVB = $var2
			foreach var1 0 5
				echo Vselect $var1
				alterparam pVA = $var1
				reset
				run
				plot A B C D Vout
			end
		end
	end
end
.endc


.lib /usr/local/share/pdk/sky130A/libs.tech/ngspice/sky130.lib.spice tt

**** end user architecture code
**.ends
.GLOBAL GND
.end
